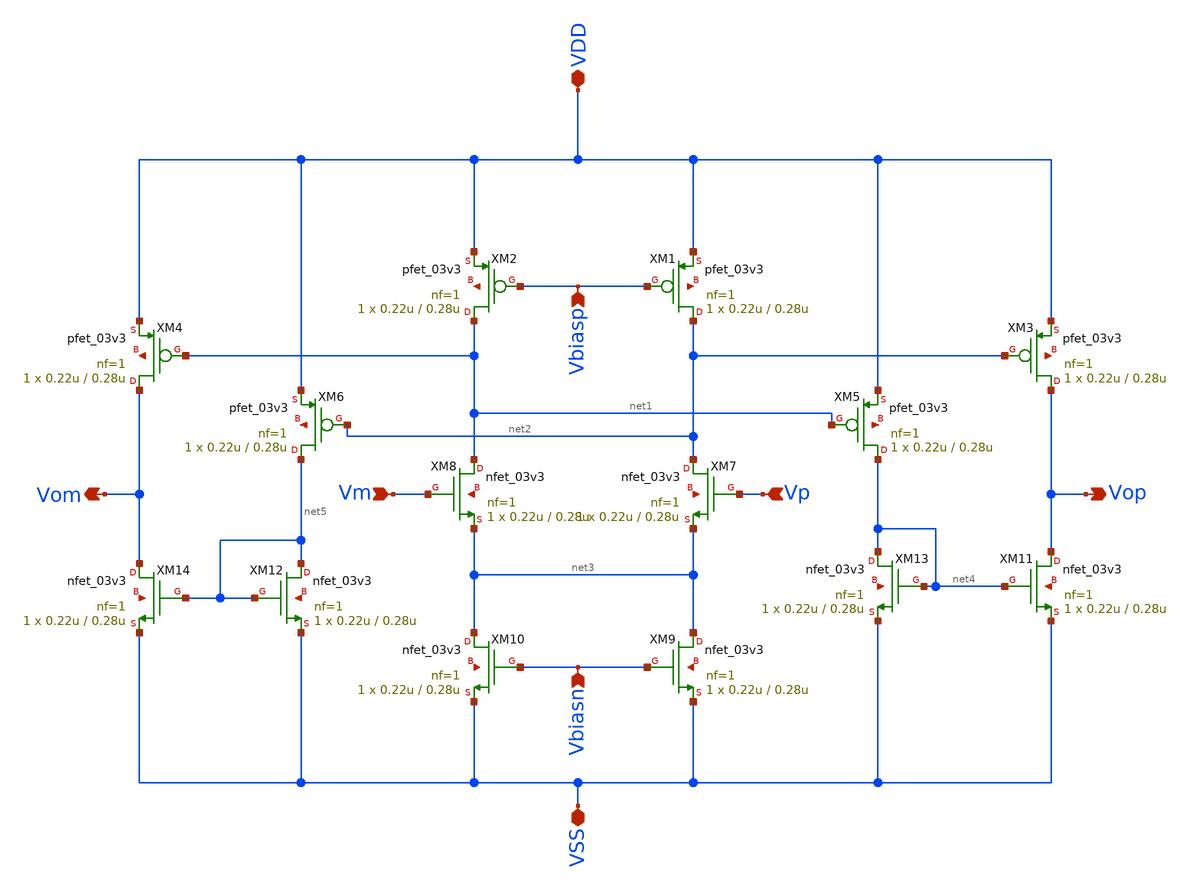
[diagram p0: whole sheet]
** sch_path: src/schematics/fullydiffamp/fullydiffamp.sch
**.subckt fullydiffamp VDD VSS Vbiasn Vbiasp Vm Vp Vom Vop
*.iopin VDD
*.iopin VSS
*.ipin Vbiasn
*.ipin Vbiasp
*.ipin Vm
*.ipin Vp
*.opin Vom
*.opin Vop
XM5 net4 net1 VDD net6 pfet_03v3 L=0.28u W=0.22u nf=1 ad='int((nf+1)/2) * W/nf * 0.18u' as='int((nf+2)/2) * W/nf * 0.18u'
+ pd='2*int((nf+1)/2) * (W/nf + 0.18u)' ps='2*int((nf+2)/2) * (W/nf + 0.18u)' nrd='0.18u / W' nrs='0.18u / W'
+ sa=0 sb=0 sd=0 m=1
XM2 net1 Vbiasp VDD net7 pfet_03v3 L=0.28u W=0.22u nf=1 ad='int((nf+1)/2) * W/nf * 0.18u' as='int((nf+2)/2) * W/nf * 0.18u'
+ pd='2*int((nf+1)/2) * (W/nf + 0.18u)' ps='2*int((nf+2)/2) * (W/nf + 0.18u)' nrd='0.18u / W' nrs='0.18u / W'
+ sa=0 sb=0 sd=0 m=1
XM8 net1 Vm net3 net8 nfet_03v3 L=0.28u W=0.22u nf=1 ad='int((nf+1)/2) * W/nf * 0.18u' as='int((nf+2)/2) * W/nf * 0.18u'
+ pd='2*int((nf+1)/2) * (W/nf + 0.18u)' ps='2*int((nf+2)/2) * (W/nf + 0.18u)' nrd='0.18u / W' nrs='0.18u / W'
+ sa=0 sb=0 sd=0 m=1
XM7 net2 Vp net3 net9 nfet_03v3 L=0.28u W=0.22u nf=1 ad='int((nf+1)/2) * W/nf * 0.18u' as='int((nf+2)/2) * W/nf * 0.18u'
+ pd='2*int((nf+1)/2) * (W/nf + 0.18u)' ps='2*int((nf+2)/2) * (W/nf + 0.18u)' nrd='0.18u / W' nrs='0.18u / W'
+ sa=0 sb=0 sd=0 m=1
XM1 net2 Vbiasp VDD net10 pfet_03v3 L=0.28u W=0.22u nf=1 ad='int((nf+1)/2) * W/nf * 0.18u' as='int((nf+2)/2) * W/nf * 0.18u'
+ pd='2*int((nf+1)/2) * (W/nf + 0.18u)' ps='2*int((nf+2)/2) * (W/nf + 0.18u)' nrd='0.18u / W' nrs='0.18u / W'
+ sa=0 sb=0 sd=0 m=1
XM6 net5 net2 VDD net11 pfet_03v3 L=0.28u W=0.22u nf=1 ad='int((nf+1)/2) * W/nf * 0.18u' as='int((nf+2)/2) * W/nf * 0.18u'
+ pd='2*int((nf+1)/2) * (W/nf + 0.18u)' ps='2*int((nf+2)/2) * (W/nf + 0.18u)' nrd='0.18u / W' nrs='0.18u / W'
+ sa=0 sb=0 sd=0 m=1
XM4 Vom net1 VDD net12 pfet_03v3 L=0.28u W=0.22u nf=1 ad='int((nf+1)/2) * W/nf * 0.18u' as='int((nf+2)/2) * W/nf * 0.18u'
+ pd='2*int((nf+1)/2) * (W/nf + 0.18u)' ps='2*int((nf+2)/2) * (W/nf + 0.18u)' nrd='0.18u / W' nrs='0.18u / W'
+ sa=0 sb=0 sd=0 m=1
XM3 Vop net2 VDD net13 pfet_03v3 L=0.28u W=0.22u nf=1 ad='int((nf+1)/2) * W/nf * 0.18u' as='int((nf+2)/2) * W/nf * 0.18u'
+ pd='2*int((nf+1)/2) * (W/nf + 0.18u)' ps='2*int((nf+2)/2) * (W/nf + 0.18u)' nrd='0.18u / W' nrs='0.18u / W'
+ sa=0 sb=0 sd=0 m=1
XM9 net3 Vbiasn VSS net14 nfet_03v3 L=0.28u W=0.22u nf=1 ad='int((nf+1)/2) * W/nf * 0.18u' as='int((nf+2)/2) * W/nf * 0.18u'
+ pd='2*int((nf+1)/2) * (W/nf + 0.18u)' ps='2*int((nf+2)/2) * (W/nf + 0.18u)' nrd='0.18u / W' nrs='0.18u / W'
+ sa=0 sb=0 sd=0 m=1
XM10 net3 Vbiasn VSS net15 nfet_03v3 L=0.28u W=0.22u nf=1 ad='int((nf+1)/2) * W/nf * 0.18u' as='int((nf+2)/2) * W/nf * 0.18u'
+ pd='2*int((nf+1)/2) * (W/nf + 0.18u)' ps='2*int((nf+2)/2) * (W/nf + 0.18u)' nrd='0.18u / W' nrs='0.18u / W'
+ sa=0 sb=0 sd=0 m=1
XM11 Vop net4 VSS net16 nfet_03v3 L=0.28u W=0.22u nf=1 ad='int((nf+1)/2) * W/nf * 0.18u' as='int((nf+2)/2) * W/nf * 0.18u'
+ pd='2*int((nf+1)/2) * (W/nf + 0.18u)' ps='2*int((nf+2)/2) * (W/nf + 0.18u)' nrd='0.18u / W' nrs='0.18u / W'
+ sa=0 sb=0 sd=0 m=1
XM13 net4 net4 VSS net17 nfet_03v3 L=0.28u W=0.22u nf=1 ad='int((nf+1)/2) * W/nf * 0.18u' as='int((nf+2)/2) * W/nf * 0.18u'
+ pd='2*int((nf+1)/2) * (W/nf + 0.18u)' ps='2*int((nf+2)/2) * (W/nf + 0.18u)' nrd='0.18u / W' nrs='0.18u / W'
+ sa=0 sb=0 sd=0 m=1
XM12 net5 net5 VSS net18 nfet_03v3 L=0.28u W=0.22u nf=1 ad='int((nf+1)/2) * W/nf * 0.18u' as='int((nf+2)/2) * W/nf * 0.18u'
+ pd='2*int((nf+1)/2) * (W/nf + 0.18u)' ps='2*int((nf+2)/2) * (W/nf + 0.18u)' nrd='0.18u / W' nrs='0.18u / W'
+ sa=0 sb=0 sd=0 m=1
XM14 Vom net5 VSS net19 nfet_03v3 L=0.28u W=0.22u nf=1 ad='int((nf+1)/2) * W/nf * 0.18u' as='int((nf+2)/2) * W/nf * 0.18u'
+ pd='2*int((nf+1)/2) * (W/nf + 0.18u)' ps='2*int((nf+2)/2) * (W/nf + 0.18u)' nrd='0.18u / W' nrs='0.18u / W'
+ sa=0 sb=0 sd=0 m=1
**.ends
.end
